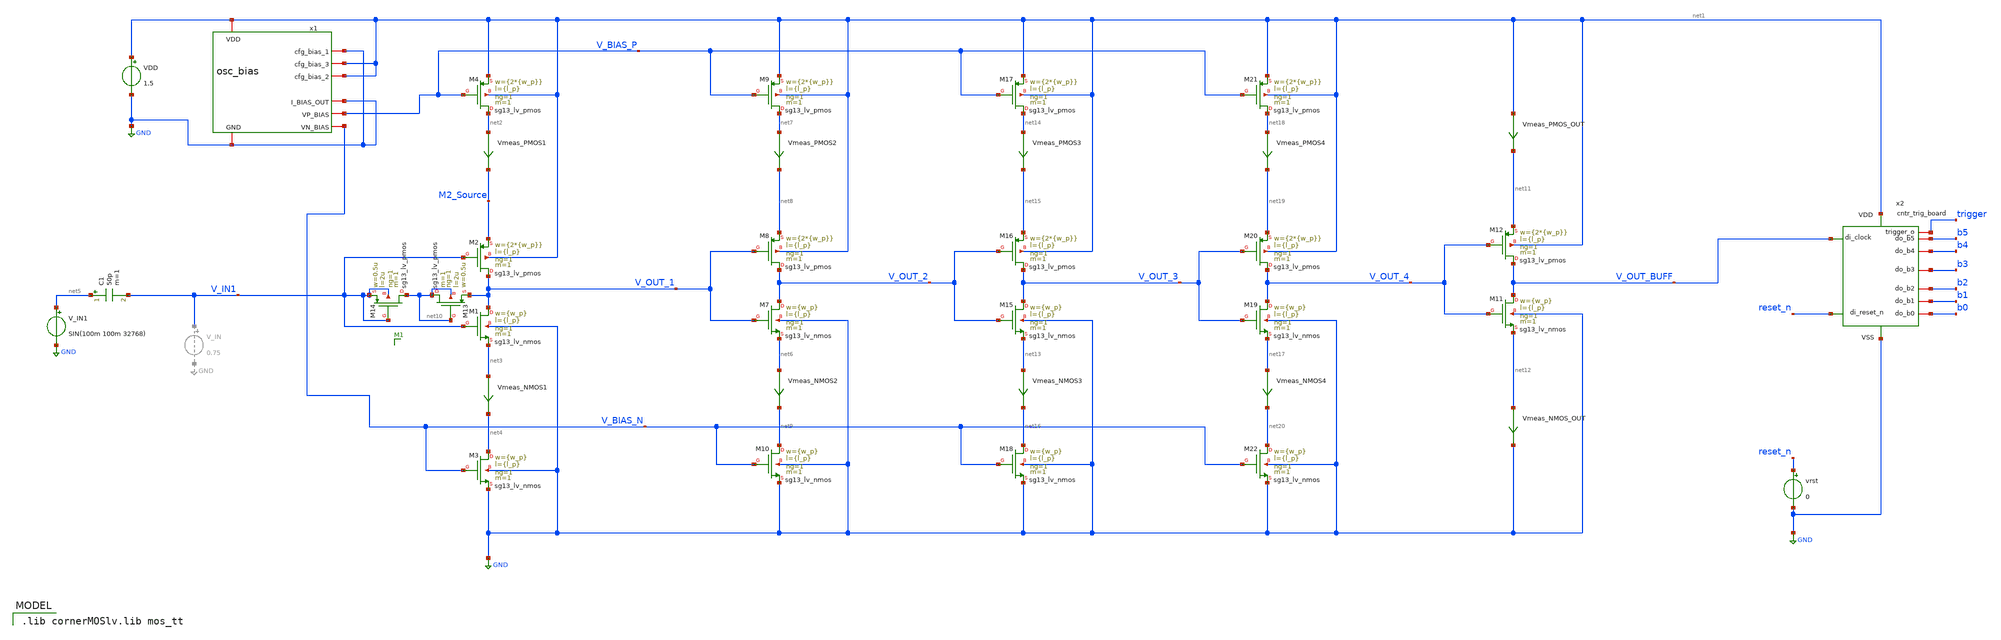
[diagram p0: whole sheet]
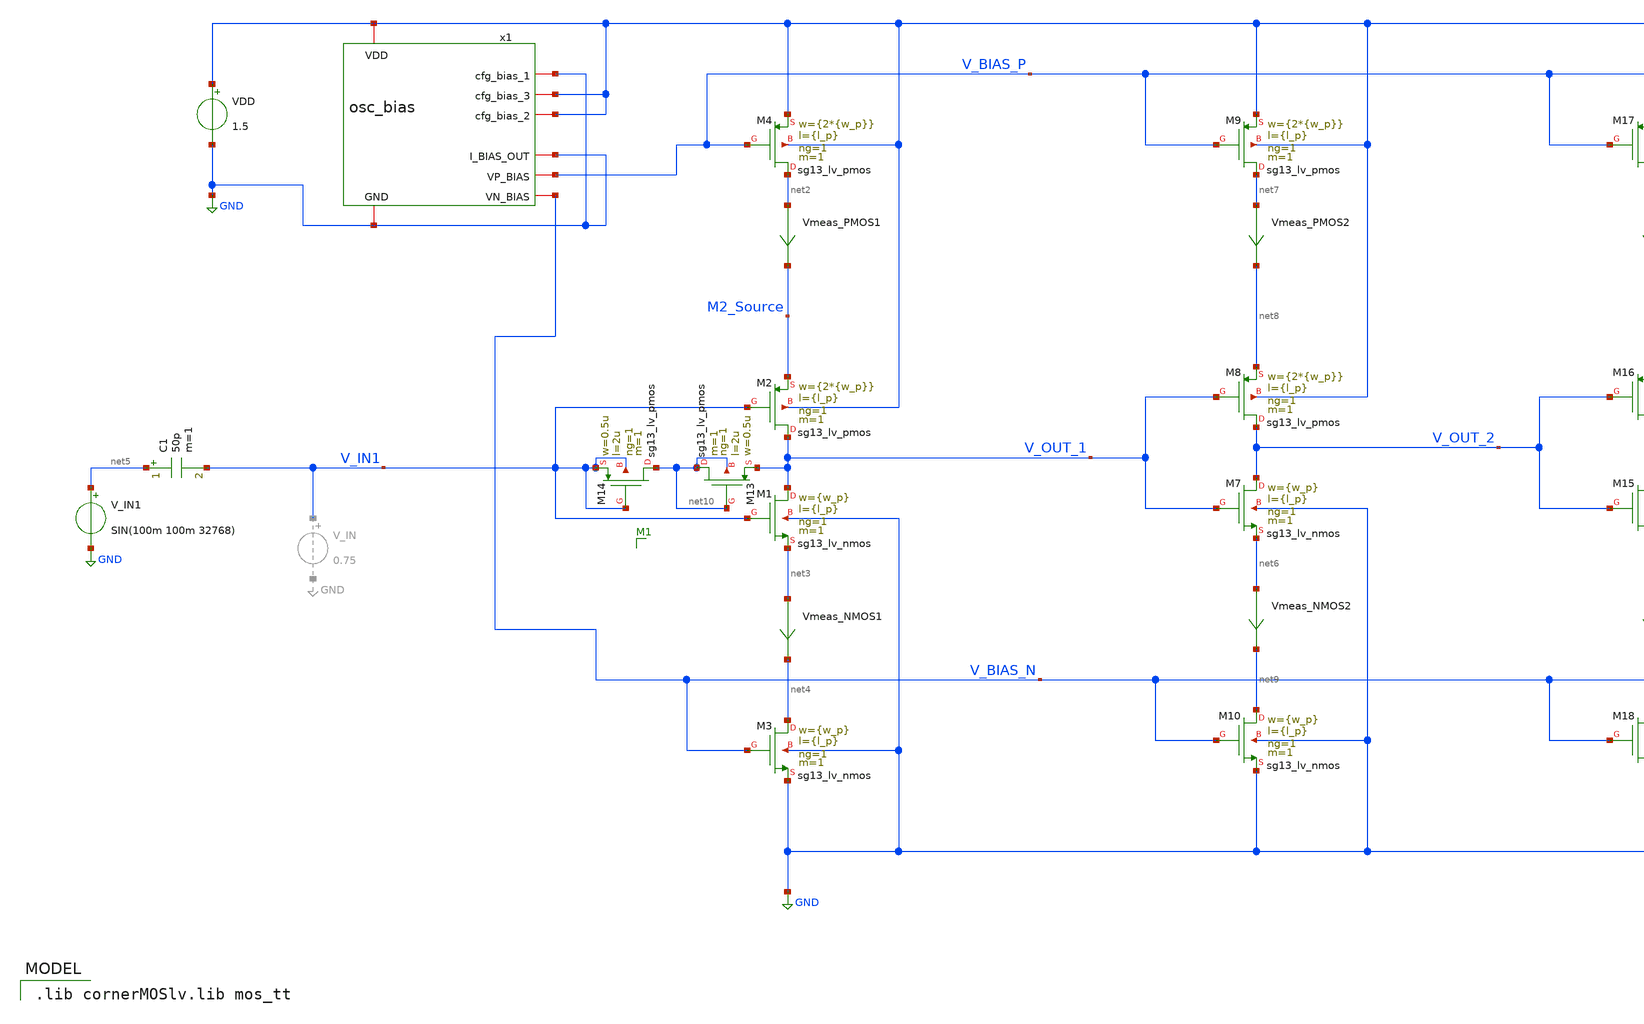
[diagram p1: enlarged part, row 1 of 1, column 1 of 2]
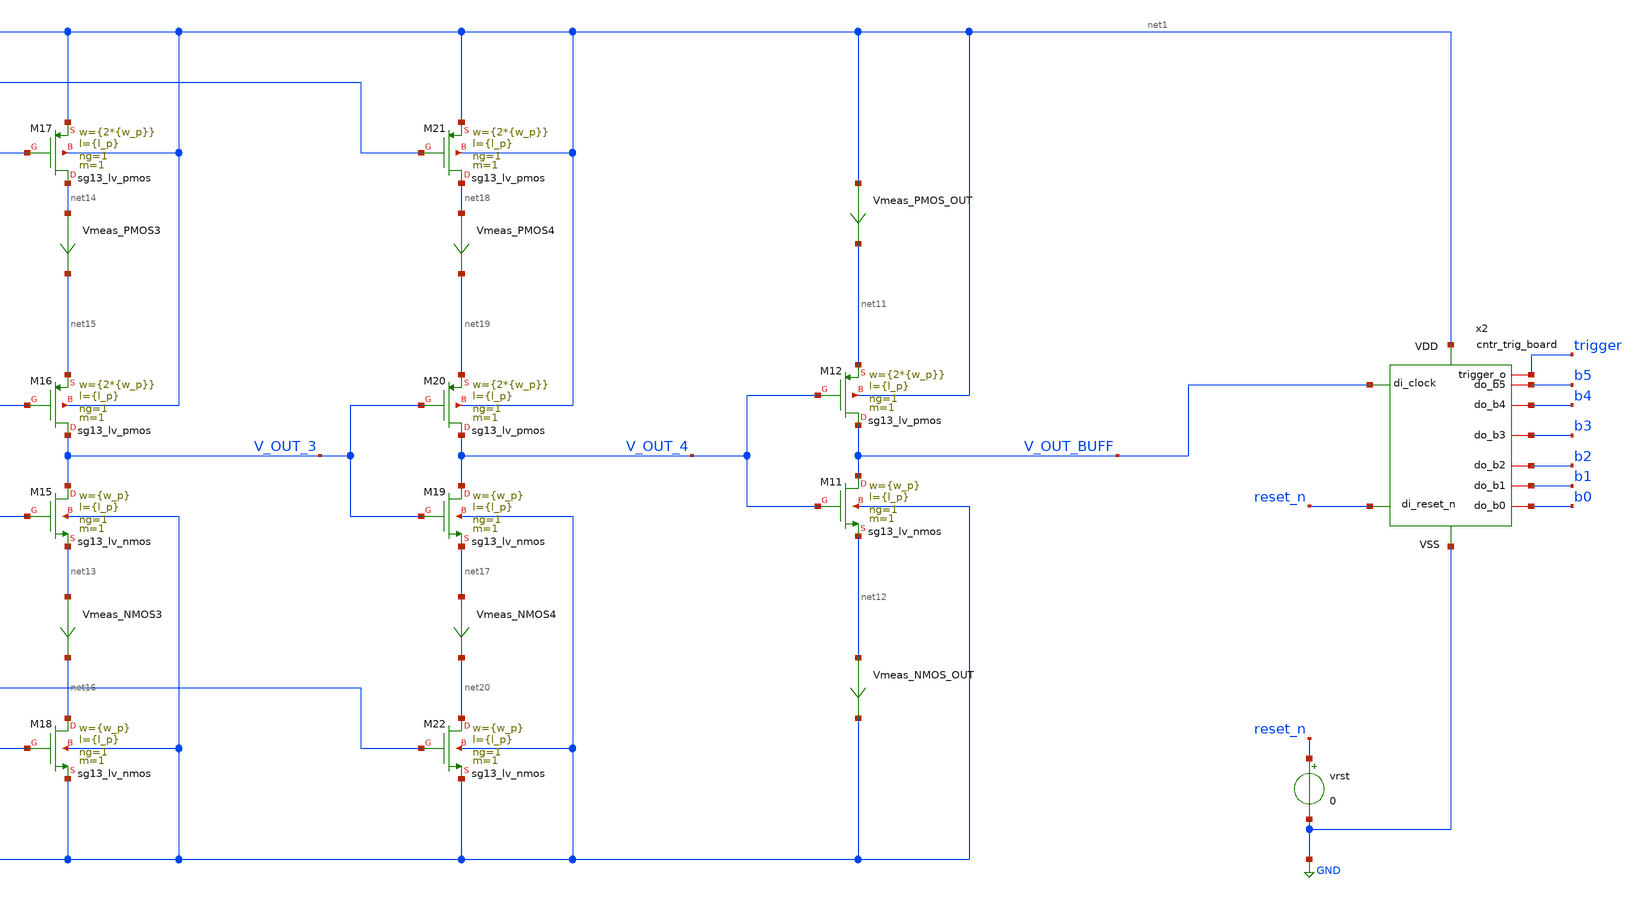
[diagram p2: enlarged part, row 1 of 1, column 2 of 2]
** sch_path: inverter_starved_v2_playground.sch
**.subckt inverter_starved_v2_playground
XM1 V_OUT_1 V_IN1 net3 GND sg13_lv_nmos w={w_p} l={l_p} ng=1 m=1 mm_ok=1
XM2 V_OUT_1 V_IN1 M2_Source net1 sg13_lv_pmos w={2*{w_p}} l={l_p} ng=1 m=1 mm_ok=1
VDD net1 GND 1.5
XM3 net4 V_BIAS_N GND GND sg13_lv_nmos w={w_p} l={l_p} ng=1 m=1 mm_ok=1
XM4 net2 V_BIAS_P net1 net1 sg13_lv_pmos w={2*{w_p}} l={l_p} ng=1 m=1 mm_ok=1
Vmeas_PMOS1 net2 M2_Source 0
.save i(vmeas_pmos1)
Vmeas_NMOS1 net3 net4 0
.save i(vmeas_nmos1)
V_IN1 net5 GND SIN(100m 100m 32768)
C1 net5 V_IN1 50p m=1
XM7 V_OUT_2 V_OUT_1 net6 GND sg13_lv_nmos w={w_p} l={l_p} ng=1 m=1 mm_ok=1
XM8 V_OUT_2 V_OUT_1 net8 net1 sg13_lv_pmos w={2*{w_p}} l={l_p} ng=1 m=1 mm_ok=1
Vmeas_NMOS2 net6 net9 0
.save i(vmeas_nmos2)
XM9 net7 V_BIAS_P net1 net1 sg13_lv_pmos w={2*{w_p}} l={l_p} ng=1 m=1 mm_ok=1
Vmeas_PMOS2 net7 net8 0
.save i(vmeas_pmos2)
XM10 net9 V_BIAS_N GND GND sg13_lv_nmos w={w_p} l={l_p} ng=1 m=1 mm_ok=1
XM11 V_OUT_BUFF V_OUT_4 net12 GND sg13_lv_nmos w={w_p} l={l_p} ng=1 m=1 mm_ok=1
XM12 V_OUT_BUFF V_OUT_4 net11 net1 sg13_lv_pmos w={2*{w_p}} l={l_p} ng=1 m=1 mm_ok=1
XM13 net10 net10 V_OUT_1 net10 sg13_lv_pmos w=0.5u l=2u ng=1 m=1 mm_ok=1
XM14 net10 V_IN1 V_IN1 V_IN1 sg13_lv_pmos w=0.5u l=2u ng=1 m=1 mm_ok=1
Vmeas_PMOS_OUT net1 net11 0
.save i(vmeas_pmos_out)
Vmeas_NMOS_OUT net12 GND 0
.save i(vmeas_nmos_out)
XM15 V_OUT_3 V_OUT_2 net13 GND sg13_lv_nmos w={w_p} l={l_p} ng=1 m=1 mm_ok=1
XM16 V_OUT_3 V_OUT_2 net15 net1 sg13_lv_pmos w={2*{w_p}} l={l_p} ng=1 m=1 mm_ok=1
Vmeas_NMOS3 net13 net16 0
.save i(vmeas_nmos3)
XM17 net14 V_BIAS_P net1 net1 sg13_lv_pmos w={2*{w_p}} l={l_p} ng=1 m=1 mm_ok=1
Vmeas_PMOS3 net14 net15 0
.save i(vmeas_pmos3)
XM18 net16 V_BIAS_N GND GND sg13_lv_nmos w={w_p} l={l_p} ng=1 m=1 mm_ok=1
XM19 V_OUT_4 V_OUT_3 net17 GND sg13_lv_nmos w={w_p} l={l_p} ng=1 m=1 mm_ok=1
XM20 V_OUT_4 V_OUT_3 net19 net1 sg13_lv_pmos w={2*{w_p}} l={l_p} ng=1 m=1 mm_ok=1
Vmeas_NMOS4 net17 net20 0
.save i(vmeas_nmos4)
XM21 net18 V_BIAS_P net1 net1 sg13_lv_pmos w={2*{w_p}} l={l_p} ng=1 m=1 mm_ok=1
Vmeas_PMOS4 net18 net19 0
.save i(vmeas_pmos4)
XM22 net20 V_BIAS_N GND GND sg13_lv_nmos w={w_p} l={l_p} ng=1 m=1 mm_ok=1
x1 net1 GND net1 net1 GND GND V_BIAS_P V_BIAS_N osc_bias
x2 net1 GND V_OUT_BUFF b0 b1 b2 b3 b4 b5 reset_n trigger cntr_trig_board
vrst reset_n GND 0
**** begin user architecture code
 .lib cornerMOSlv.lib mos_tt



.include inverter_starved_v2_playground.save
.include /foss/designs/xtal/xspice/cntr_trig_board.xspice
.param w_p=0.40u l_p=0.13u
.meas tran iavg_stage_1_pmos AVG i(Vmeas_PMOS1)
.meas tran iavg_stage_1_nmos AVG i(Vmeas_NMOS2)
.meas tran iavg_stage_2_pmos AVG i(Vmeas_PMOS2)
.meas tran iavg_stage_2_nmos AVG i(Vmeas_NMOS2)
.meas tran iavg_stage_3_pmos AVG i(Vmeas_PMOS3)
.meas tran iavg_stage_3_nmos AVG i(Vmeas_NMOS3)
.meas tran iavg_stage_4_pmos AVG i(Vmeas_PMOS4)
.meas tran iavg_stage_4_nmos AVG i(Vmeas_NMOS4)
.meas tran iavg_stage_5_pmos AVG i(Vmeas_PMOS_OUT)
.meas tran iavg_stage_5_nmos AVG i(Vmeas_NMOS_OUT)
.meas tran iavg_VDD AVG i(VDD)

.control
save all


tran 0.1u 2m
write inverter_starved_v2_playground.raw

*plot V_IN1 V_OUT_1 V_OUT_2 V_OUT_3 V_OUT_4 V_OUT_BUFF
plot V_IN1 V_OUT_BUFF


*fft V_OUT_3
*plot mag(V_OUT_3)

*.measure tran yrms RMS i(VDD) from=0.1m to=0.2m

.endc


**** end user architecture code
**.ends

* expanding   symbol:  osc_bias.sym # of pins=8
** sym_path: osc_bias.sym
** sch_path: osc_bias.sch
.subckt osc_bias VDD cfg_bias_1 cfg_bias_3 cfg_bias_2 GND I_BIAS_OUT VP_BIAS VN_BIAS
*.iopin VDD
*.iopin GND
*.iopin I_BIAS_OUT
*.iopin cfg_bias_1
*.iopin cfg_bias_2
*.iopin cfg_bias_3
*.opin VN_BIAS
*.opin VP_BIAS
XM1 net1 net1 VDD VDD sg13_lv_pmos w=0.25u l=10u ng=1 m=1 mm_ok=1
XM3 net1 net1 net2 GND sg13_lv_nmos w=0.25u l=10u ng=1 m=1 mm_ok=1
XM4 net2 net2 net3 GND sg13_lv_nmos w=0.25u l=10u ng=1 m=1 mm_ok=1
XM5 net3 net3 net14 GND sg13_lv_nmos w=0.25u l=10u ng=1 m=1 mm_ok=1
XM2 net9 net1 VDD VDD sg13_lv_pmos w=0.25u l=10u ng=1 m=2 mm_ok=1
XM6 net4 cfg_bias_1 net9 VDD sg13_lv_pmos w=0.25u l=10u ng=1 m=1 mm_ok=1
XM7 net5 net1 VDD VDD sg13_lv_pmos w=0.25u l=10u ng=1 m=4 mm_ok=1
XM8 net6 net1 VDD VDD sg13_lv_pmos w=0.25u l=10u ng=1 m=20 mm_ok=1
XM9 net4 cfg_bias_2 net5 VDD sg13_lv_pmos w=0.5u l=10u ng=1 m=1 mm_ok=1
XM10 net4 cfg_bias_3 net6 VDD sg13_lv_pmos w=1u l=10u ng=1 m=1 mm_ok=1
XM11 net7 net7 net8 GND sg13_lv_nmos w=0.2u l=10u ng=1 m=1 mm_ok=1
Vmeas net8 GND 0
.save i(vmeas)
XM12 VP_BIAS VP_BIAS net12 VDD sg13_lv_pmos w=0.8u l=0.13u ng=1 m=1 mm_ok=1
XM13 VN_BIAS VN_BIAS net11 GND sg13_lv_nmos w=0.4u l=0.13u ng=1 m=1 mm_ok=1
Vmeas1 VDD net12 0
.save i(vmeas1)
Vmeas2 net11 GND 0
.save i(vmeas2)
XM14 net10 net10 VN_BIAS GND sg13_lv_nmos w=0.4u l=10u ng=1 m=1 mm_ok=1
XM15 net13 net13 net10 GND sg13_lv_nmos w=0.4u l=10u ng=1 m=1 mm_ok=1
XM16 VP_BIAS VP_BIAS net13 GND sg13_lv_nmos w=0.4u l=10u ng=1 m=1 mm_ok=1
XM17 net14 net14 net7 GND sg13_lv_nmos w=0.25u l=10u ng=1 m=1 mm_ok=1
Vmeas3 net4 I_BIAS_OUT 0
.save i(vmeas3)
.ends

.GLOBAL GND
.end
